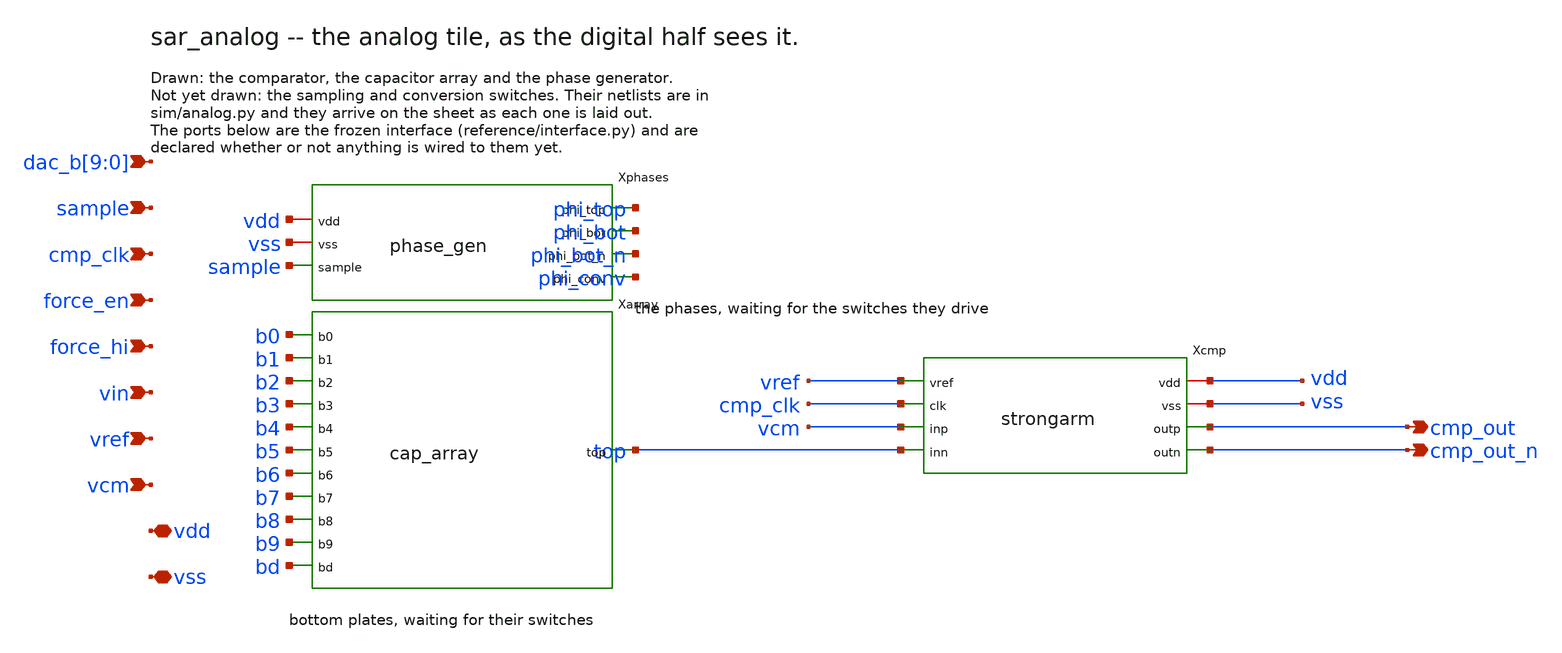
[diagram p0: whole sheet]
** sch_path: xschem/sar_analog.sch
**.subckt sar_analog
*+ dac_b[9],dac_b[8],dac_b[7],dac_b[6],dac_b[5],dac_b[4],dac_b[3],dac_b[2],dac_b[1],dac_b[0] sample cmp_clk force_en force_hi vin vref vcm vdd vss cmp_out cmp_out_n
*.ipin dac_b[9],dac_b[8],dac_b[7],dac_b[6],dac_b[5],dac_b[4],dac_b[3],dac_b[2],dac_b[1],dac_b[0]
*.ipin sample
*.ipin cmp_clk
*.ipin force_en
*.ipin force_hi
*.ipin vin
*.ipin vref
*.ipin vcm
*.iopin vdd
*.iopin vss
*.opin cmp_out
*.opin cmp_out_n
Xcmp vdd vss vref cmp_clk vcm top cmp_out cmp_out_n strongarm
Xphases vdd vss sample phi_top phi_bot phi_bot_n phi_conv phase_gen
Xarray top b0 b1 b2 b3 b4 b5 b6 b7 b8 b9 bd cap_array
**.ends

* expanding   symbol:  strongarm.sym # of pins=8
** sym_path: xschem/strongarm.sym
** sch_path: xschem/strongarm.sch
.subckt strongarm vdd vss vref clk inp inn outp outn
*.iopin vdd
*.iopin vss
*.ipin vref
*.ipin clk
*.ipin inp
*.ipin inn
*.opin outp
*.opin outn
Xinvp clk_i clk vdd vdd sky130_fd_pr__pfet_01v8 L=0.15 W=2 nf=1 ad='int((nf+1)/2) * W/nf * 0.29' as='int((nf+2)/2) * W/nf * 0.29'
+ pd='2*int((nf+1)/2) * (W/nf + 0.29)' ps='2*int((nf+2)/2) * (W/nf + 0.29)' nrd='0.29 / W' nrs='0.29 / W'
+ sa=0 sb=0 sd=0 mult=1 m=1
Xinvn clk_i clk vss vss sky130_fd_pr__nfet_01v8 L=0.15 W=2 nf=1 ad='int((1 + 1)/2) * 2 / 1 * 0.29' as='int((1 + 2)/2) * 2 / 1 * 0.29'
+ pd='2*int((1 + 1)/2) * (2 / 1 + 0.29)' ps='2*int((1 + 2)/2) * (2 / 1 + 0.29)' nrd='0.29 / 2 ' nrs='0.29 / 2 '
+ sa=0 sb=0 sd=0 mult=1 m=1
Xbref bias vref vss vss sky130_fd_pr__nfet_01v8 L=2 W=1 nf=1 ad='int((1 + 1)/2) * 1 / 1 * 0.29' as='int((1 + 2)/2) * 1 / 1 * 0.29'
+ pd='2*int((1 + 1)/2) * (1 / 1 + 0.29)' ps='2*int((1 + 2)/2) * (1 / 1 + 0.29)' nrd='0.29 / 1 ' nrs='0.29 / 1 '
+ sa=0 sb=0 sd=0 mult=1 m=1
Xbdio bias bias vdd vdd sky130_fd_pr__pfet_01v8 L=0.5 W=1 nf=1 ad='int((nf+1)/2) * W/nf * 0.29' as='int((nf+2)/2) * W/nf * 0.29'
+ pd='2*int((nf+1)/2) * (W/nf + 0.29)' ps='2*int((nf+2)/2) * (W/nf + 0.29)' nrd='0.29 / W' nrs='0.29 / W'
+ sa=0 sb=0 sd=0 mult=1 m=1
Xbgoff tgate clk vdd vdd sky130_fd_pr__pfet_01v8 L=0.15 W=1 nf=1 ad='int((nf+1)/2) * W/nf * 0.29' as='int((nf+2)/2) * W/nf * 0.29'
+ pd='2*int((nf+1)/2) * (W/nf + 0.29)' ps='2*int((nf+2)/2) * (W/nf + 0.29)' nrd='0.29 / W' nrs='0.29 / W'
+ sa=0 sb=0 sd=0 mult=1 m=1
Xbgon bias clk tgate vss sky130_fd_pr__nfet_01v8 L=0.15 W=1 nf=1 ad='int((1 + 1)/2) * 1 / 1 * 0.29' as='int((1 + 2)/2) * 1 / 1 * 0.29'
+ pd='2*int((1 + 1)/2) * (1 / 1 + 0.29)' ps='2*int((1 + 2)/2) * (1 / 1 + 0.29)' nrd='0.29 / 1 ' nrs='0.29 / 1 '
+ sa=0 sb=0 sd=0 mult=1 m=1
Cbias bias vss 1e-13 m=1
Xtail tail tgate vdd vdd sky130_fd_pr__pfet_01v8 L=0.5 W=2 nf=1 ad='int((nf+1)/2) * W/nf * 0.29' as='int((nf+2)/2) * W/nf * 0.29'
+ pd='2*int((nf+1)/2) * (W/nf + 0.29)' ps='2*int((nf+2)/2) * (W/nf + 0.29)' nrd='0.29 / W' nrs='0.29 / W'
+ sa=0 sb=0 sd=0 mult=1 m=1
Xinp xn inp tail vdd sky130_fd_pr__pfet_01v8 L=0.5 W=4 nf=1 ad='int((nf+1)/2) * W/nf * 0.29' as='int((nf+2)/2) * W/nf * 0.29'
+ pd='2*int((nf+1)/2) * (W/nf + 0.29)' ps='2*int((nf+2)/2) * (W/nf + 0.29)' nrd='0.29 / W' nrs='0.29 / W'
+ sa=0 sb=0 sd=0 mult=1 m=1
Xinn xp inn tail vdd sky130_fd_pr__pfet_01v8 L=0.5 W=4 nf=1 ad='int((nf+1)/2) * W/nf * 0.29' as='int((nf+2)/2) * W/nf * 0.29'
+ pd='2*int((nf+1)/2) * (W/nf + 0.29)' ps='2*int((nf+2)/2) * (W/nf + 0.29)' nrd='0.29 / W' nrs='0.29 / W'
+ sa=0 sb=0 sd=0 mult=1 m=1
Xlchp outp outn xp vdd sky130_fd_pr__pfet_01v8 L=0.15 W=1 nf=1 ad='int((nf+1)/2) * W/nf * 0.29' as='int((nf+2)/2) * W/nf * 0.29'
+ pd='2*int((nf+1)/2) * (W/nf + 0.29)' ps='2*int((nf+2)/2) * (W/nf + 0.29)' nrd='0.29 / W' nrs='0.29 / W'
+ sa=0 sb=0 sd=0 mult=1 m=1
Xlchn outn outp xn vdd sky130_fd_pr__pfet_01v8 L=0.15 W=1 nf=1 ad='int((nf+1)/2) * W/nf * 0.29' as='int((nf+2)/2) * W/nf * 0.29'
+ pd='2*int((nf+1)/2) * (W/nf + 0.29)' ps='2*int((nf+2)/2) * (W/nf + 0.29)' nrd='0.29 / W' nrs='0.29 / W'
+ sa=0 sb=0 sd=0 mult=1 m=1
Xldp outp outn vss vss sky130_fd_pr__nfet_01v8 L=0.15 W=2 nf=1 ad='int((1 + 1)/2) * 2 / 1 * 0.29' as='int((1 + 2)/2) * 2 / 1 * 0.29'
+ pd='2*int((1 + 1)/2) * (2 / 1 + 0.29)' ps='2*int((1 + 2)/2) * (2 / 1 + 0.29)' nrd='0.29 / 2 ' nrs='0.29 / 2 '
+ sa=0 sb=0 sd=0 mult=1 m=1
Xldn outn outp vss vss sky130_fd_pr__nfet_01v8 L=0.15 W=2 nf=1 ad='int((1 + 1)/2) * 2 / 1 * 0.29' as='int((1 + 2)/2) * 2 / 1 * 0.29'
+ pd='2*int((1 + 1)/2) * (2 / 1 + 0.29)' ps='2*int((1 + 2)/2) * (2 / 1 + 0.29)' nrd='0.29 / 2 ' nrs='0.29 / 2 '
+ sa=0 sb=0 sd=0 mult=1 m=1
Xprep outp clk_i vss vss sky130_fd_pr__nfet_01v8 L=0.15 W=2 nf=1 ad='int((1 + 1)/2) * 2 / 1 * 0.29' as='int((1 + 2)/2) * 2 / 1 * 0.29'
+ pd='2*int((1 + 1)/2) * (2 / 1 + 0.29)' ps='2*int((1 + 2)/2) * (2 / 1 + 0.29)' nrd='0.29 / 2 ' nrs='0.29 / 2 '
+ sa=0 sb=0 sd=0 mult=1 m=1
Xpren outn clk_i vss vss sky130_fd_pr__nfet_01v8 L=0.15 W=2 nf=1 ad='int((1 + 1)/2) * 2 / 1 * 0.29' as='int((1 + 2)/2) * 2 / 1 * 0.29'
+ pd='2*int((1 + 1)/2) * (2 / 1 + 0.29)' ps='2*int((1 + 2)/2) * (2 / 1 + 0.29)' nrd='0.29 / 2 ' nrs='0.29 / 2 '
+ sa=0 sb=0 sd=0 mult=1 m=1
Xprxp xp clk_i vss vss sky130_fd_pr__nfet_01v8 L=0.15 W=2 nf=1 ad='int((1 + 1)/2) * 2 / 1 * 0.29' as='int((1 + 2)/2) * 2 / 1 * 0.29'
+ pd='2*int((1 + 1)/2) * (2 / 1 + 0.29)' ps='2*int((1 + 2)/2) * (2 / 1 + 0.29)' nrd='0.29 / 2 ' nrs='0.29 / 2 '
+ sa=0 sb=0 sd=0 mult=1 m=1
Xprxn xn clk_i vss vss sky130_fd_pr__nfet_01v8 L=0.15 W=2 nf=1 ad='int((1 + 1)/2) * 2 / 1 * 0.29' as='int((1 + 2)/2) * 2 / 1 * 0.29'
+ pd='2*int((1 + 1)/2) * (2 / 1 + 0.29)' ps='2*int((1 + 2)/2) * (2 / 1 + 0.29)' nrd='0.29 / 2 ' nrs='0.29 / 2 '
+ sa=0 sb=0 sd=0 mult=1 m=1
Cxp xp vss 2e-13 m=1
Cxn xn vss 2e-13 m=1
Coutp outp vss 1e-14 m=1
Coutn outn vss 1e-14 m=1
.ends


* expanding   symbol:  phase_gen.sym # of pins=7
** sym_path: xschem/phase_gen.sym
** sch_path: xschem/phase_gen.sch
.subckt phase_gen vdd vss sample phi_top phi_bot phi_bot_n phi_conv
*.iopin vdd
*.iopin vss
*.ipin sample
*.opin phi_top
*.opin phi_bot
*.opin phi_bot_n
*.opin phi_conv
Xbtop0p btop_s0 sample vdd vdd sky130_fd_pr__pfet_01v8 L=0.15 W=1 nf=1 ad='int((nf+1)/2) * W/nf * 0.29'
+ as='int((nf+2)/2) * W/nf * 0.29' pd='2*int((nf+1)/2) * (W/nf + 0.29)' ps='2*int((nf+2)/2) * (W/nf + 0.29)'
+ nrd='0.29 / W' nrs='0.29 / W' sa=0 sb=0 sd=0 mult=1 m=1
Xbtop0n btop_s0 sample vss vss sky130_fd_pr__nfet_01v8 L=0.15 W=0.5 nf=1 ad='int((1 + 1)/2) * 0.5 / 1 * 0.29'
+ as='int((1 + 2)/2) * 0.5 / 1 * 0.29' pd='2*int((1 + 1)/2) * (0.5 / 1 + 0.29)' ps='2*int((1 + 2)/2) * (0.5 / 1 + 0.29)'
+ nrd='0.29 / 0.5 ' nrs='0.29 / 0.5 ' sa=0 sb=0 sd=0 mult=1 m=1
Xbtop1p phi_top btop_s0 vdd vdd sky130_fd_pr__pfet_01v8 L=0.15 W=4 nf=1 ad='int((nf+1)/2) * W/nf * 0.29'
+ as='int((nf+2)/2) * W/nf * 0.29' pd='2*int((nf+1)/2) * (W/nf + 0.29)' ps='2*int((nf+2)/2) * (W/nf + 0.29)'
+ nrd='0.29 / W' nrs='0.29 / W' sa=0 sb=0 sd=0 mult=1 m=1
Xbtop1n phi_top btop_s0 vss vss sky130_fd_pr__nfet_01v8 L=0.15 W=2 nf=1 ad='int((1 + 1)/2) * 2 / 1 * 0.29'
+ as='int((1 + 2)/2) * 2 / 1 * 0.29' pd='2*int((1 + 1)/2) * (2 / 1 + 0.29)' ps='2*int((1 + 2)/2) * (2 / 1 + 0.29)'
+ nrd='0.29 / 2 ' nrs='0.29 / 2 ' sa=0 sb=0 sd=0 mult=1 m=1
Xstopsp stop_lo phi_top vdd vdd sky130_fd_pr__pfet_01v8 L=1 W=0.42 nf=1 ad='int((nf+1)/2) * W/nf * 0.29'
+ as='int((nf+2)/2) * W/nf * 0.29' pd='2*int((nf+1)/2) * (W/nf + 0.29)' ps='2*int((nf+2)/2) * (W/nf + 0.29)'
+ nrd='0.29 / W' nrs='0.29 / W' sa=0 sb=0 sd=0 mult=1 m=1
Xstopsn stop_lo phi_top vss vss sky130_fd_pr__nfet_01v8 L=0.15 W=2 nf=1 ad='int((1 + 1)/2) * 2 / 1 * 0.29'
+ as='int((1 + 2)/2) * 2 / 1 * 0.29' pd='2*int((1 + 1)/2) * (2 / 1 + 0.29)' ps='2*int((1 + 2)/2) * (2 / 1 + 0.29)'
+ nrd='0.29 / 2 ' nrs='0.29 / 2 ' sa=0 sb=0 sd=0 mult=1 m=1
Xstoprp top_on stop_lo vdd vdd sky130_fd_pr__pfet_01v8 L=0.15 W=1 nf=1 ad='int((nf+1)/2) * W/nf * 0.29'
+ as='int((nf+2)/2) * W/nf * 0.29' pd='2*int((nf+1)/2) * (W/nf + 0.29)' ps='2*int((nf+2)/2) * (W/nf + 0.29)'
+ nrd='0.29 / W' nrs='0.29 / W' sa=0 sb=0 sd=0 mult=1 m=1
Xstoprn top_on stop_lo vss vss sky130_fd_pr__nfet_01v8 L=0.15 W=0.5 nf=1 ad='int((1 + 1)/2) * 0.5 / 1 * 0.29'
+ as='int((1 + 2)/2) * 0.5 / 1 * 0.29' pd='2*int((1 + 1)/2) * (0.5 / 1 + 0.29)' ps='2*int((1 + 2)/2) * (0.5 / 1 + 0.29)'
+ nrd='0.29 / 0.5 ' nrs='0.29 / 0.5 ' sa=0 sb=0 sd=0 mult=1 m=1
Xnor_heldp0 nor_held_m0 sample vdd vdd sky130_fd_pr__pfet_01v8 L=0.15 W=2 nf=1 ad='int((nf+1)/2) * W/nf * 0.29'
+ as='int((nf+2)/2) * W/nf * 0.29' pd='2*int((nf+1)/2) * (W/nf + 0.29)' ps='2*int((nf+2)/2) * (W/nf + 0.29)'
+ nrd='0.29 / W' nrs='0.29 / W' sa=0 sb=0 sd=0 mult=1 m=1
Xnor_heldp1 held_n top_on nor_held_m0 vdd sky130_fd_pr__pfet_01v8 L=0.15 W=2 nf=1 ad='int((nf+1)/2) * W/nf * 0.29'
+ as='int((nf+2)/2) * W/nf * 0.29' pd='2*int((nf+1)/2) * (W/nf + 0.29)' ps='2*int((nf+2)/2) * (W/nf + 0.29)'
+ nrd='0.29 / W' nrs='0.29 / W' sa=0 sb=0 sd=0 mult=1 m=1
Xnor_heldn0 held_n sample vss vss sky130_fd_pr__nfet_01v8 L=0.15 W=0.5 nf=1 ad='int((1 + 1)/2) * 0.5 / 1 * 0.29'
+ as='int((1 + 2)/2) * 0.5 / 1 * 0.29' pd='2*int((1 + 1)/2) * (0.5 / 1 + 0.29)' ps='2*int((1 + 2)/2) * (0.5 / 1 + 0.29)'
+ nrd='0.29 / 0.5 ' nrs='0.29 / 0.5 ' sa=0 sb=0 sd=0 mult=1 m=1
Xnor_heldn1 held_n top_on vss vss sky130_fd_pr__nfet_01v8 L=0.15 W=0.5 nf=1 ad='int((1 + 1)/2) * 0.5 / 1 * 0.29'
+ as='int((1 + 2)/2) * 0.5 / 1 * 0.29' pd='2*int((1 + 1)/2) * (0.5 / 1 + 0.29)' ps='2*int((1 + 2)/2) * (0.5 / 1 + 0.29)'
+ nrd='0.29 / 0.5 ' nrs='0.29 / 0.5 ' sa=0 sb=0 sd=0 mult=1 m=1
Xnor_botp0 nor_bot_m0 held_n vdd vdd sky130_fd_pr__pfet_01v8 L=0.15 W=2 nf=1 ad='int((nf+1)/2) * W/nf * 0.29'
+ as='int((nf+2)/2) * W/nf * 0.29' pd='2*int((nf+1)/2) * (W/nf + 0.29)' ps='2*int((nf+2)/2) * (W/nf + 0.29)'
+ nrd='0.29 / W' nrs='0.29 / W' sa=0 sb=0 sd=0 mult=1 m=1
Xnor_botp1 bot_pre cnv_on nor_bot_m0 vdd sky130_fd_pr__pfet_01v8 L=0.15 W=2 nf=1 ad='int((nf+1)/2) * W/nf * 0.29'
+ as='int((nf+2)/2) * W/nf * 0.29' pd='2*int((nf+1)/2) * (W/nf + 0.29)' ps='2*int((nf+2)/2) * (W/nf + 0.29)'
+ nrd='0.29 / W' nrs='0.29 / W' sa=0 sb=0 sd=0 mult=1 m=1
Xnor_botn0 bot_pre held_n vss vss sky130_fd_pr__nfet_01v8 L=0.15 W=0.5 nf=1 ad='int((1 + 1)/2) * 0.5 / 1 * 0.29'
+ as='int((1 + 2)/2) * 0.5 / 1 * 0.29' pd='2*int((1 + 1)/2) * (0.5 / 1 + 0.29)' ps='2*int((1 + 2)/2) * (0.5 / 1 + 0.29)'
+ nrd='0.29 / 0.5 ' nrs='0.29 / 0.5 ' sa=0 sb=0 sd=0 mult=1 m=1
Xnor_botn1 bot_pre cnv_on vss vss sky130_fd_pr__nfet_01v8 L=0.15 W=0.5 nf=1 ad='int((1 + 1)/2) * 0.5 / 1 * 0.29'
+ as='int((1 + 2)/2) * 0.5 / 1 * 0.29' pd='2*int((1 + 1)/2) * (0.5 / 1 + 0.29)' ps='2*int((1 + 2)/2) * (0.5 / 1 + 0.29)'
+ nrd='0.29 / 0.5 ' nrs='0.29 / 0.5 ' sa=0 sb=0 sd=0 mult=1 m=1
Xbbot0p bbot_s0 bot_pre vdd vdd sky130_fd_pr__pfet_01v8 L=0.15 W=1 nf=1 ad='int((nf+1)/2) * W/nf * 0.29'
+ as='int((nf+2)/2) * W/nf * 0.29' pd='2*int((nf+1)/2) * (W/nf + 0.29)' ps='2*int((nf+2)/2) * (W/nf + 0.29)'
+ nrd='0.29 / W' nrs='0.29 / W' sa=0 sb=0 sd=0 mult=1 m=1
Xbbot0n bbot_s0 bot_pre vss vss sky130_fd_pr__nfet_01v8 L=0.15 W=0.5 nf=1 ad='int((1 + 1)/2) * 0.5 / 1 * 0.29'
+ as='int((1 + 2)/2) * 0.5 / 1 * 0.29' pd='2*int((1 + 1)/2) * (0.5 / 1 + 0.29)' ps='2*int((1 + 2)/2) * (0.5 / 1 + 0.29)'
+ nrd='0.29 / 0.5 ' nrs='0.29 / 0.5 ' sa=0 sb=0 sd=0 mult=1 m=1
Xbbot1p bbot_s1 bbot_s0 vdd vdd sky130_fd_pr__pfet_01v8 L=0.15 W=4 nf=1 ad='int((nf+1)/2) * W/nf * 0.29'
+ as='int((nf+2)/2) * W/nf * 0.29' pd='2*int((nf+1)/2) * (W/nf + 0.29)' ps='2*int((nf+2)/2) * (W/nf + 0.29)'
+ nrd='0.29 / W' nrs='0.29 / W' sa=0 sb=0 sd=0 mult=1 m=1
Xbbot1n bbot_s1 bbot_s0 vss vss sky130_fd_pr__nfet_01v8 L=0.15 W=2 nf=1 ad='int((1 + 1)/2) * 2 / 1 * 0.29'
+ as='int((1 + 2)/2) * 2 / 1 * 0.29' pd='2*int((1 + 1)/2) * (2 / 1 + 0.29)' ps='2*int((1 + 2)/2) * (2 / 1 + 0.29)'
+ nrd='0.29 / 2 ' nrs='0.29 / 2 ' sa=0 sb=0 sd=0 mult=1 m=1
Xbbot2p bbot_s2 bbot_s1 vdd vdd sky130_fd_pr__pfet_01v8 L=0.15 W=4 nf=1 ad='int((nf+1)/2) * W/nf * 0.29'
+ as='int((nf+2)/2) * W/nf * 0.29' pd='2*int((nf+1)/2) * (W/nf + 0.29)' ps='2*int((nf+2)/2) * (W/nf + 0.29)'
+ nrd='0.29 / W' nrs='0.29 / W' sa=0 sb=0 sd=0 mult=4 m=4
Xbbot2n bbot_s2 bbot_s1 vss vss sky130_fd_pr__nfet_01v8 L=0.15 W=4 nf=1 ad='int((1 + 1)/2) * 4 / 1 * 0.29'
+ as='int((1 + 2)/2) * 4 / 1 * 0.29' pd='2*int((1 + 1)/2) * (4 / 1 + 0.29)' ps='2*int((1 + 2)/2) * (4 / 1 + 0.29)'
+ nrd='0.29 / 4 ' nrs='0.29 / 4 ' sa=0 sb=0 sd=0 mult=2 m=2
Xbbot3p phi_bot bbot_s2 vdd vdd sky130_fd_pr__pfet_01v8 L=0.15 W=4.92308 nf=1 ad='int((nf+1)/2) * W/nf * 0.29'
+ as='int((nf+2)/2) * W/nf * 0.29' pd='2*int((nf+1)/2) * (W/nf + 0.29)' ps='2*int((nf+2)/2) * (W/nf + 0.29)'
+ nrd='0.29 / W' nrs='0.29 / W' sa=0 sb=0 sd=0 mult=13 m=13
Xbbot3n phi_bot bbot_s2 vss vss sky130_fd_pr__nfet_01v8 L=0.15 W=4.57143 nf=1 ad='int((1 + 1)/2) * 4.57143 / 1 * 0.29'
+ as='int((1 + 2)/2) * 4.57143 / 1 * 0.29' pd='2*int((1 + 1)/2) * (4.57143 / 1 + 0.29)' ps='2*int((1 + 2)/2) * (4.57143 / 1 + 0.29)'
+ nrd='0.29 / 4.57143 ' nrs='0.29 / 4.57143 ' sa=0 sb=0 sd=0 mult=7 m=7
Xsbotsp sbot_lo phi_bot vdd vdd sky130_fd_pr__pfet_01v8 L=1 W=0.42 nf=1 ad='int((nf+1)/2) * W/nf * 0.29'
+ as='int((nf+2)/2) * W/nf * 0.29' pd='2*int((nf+1)/2) * (W/nf + 0.29)' ps='2*int((nf+2)/2) * (W/nf + 0.29)'
+ nrd='0.29 / W' nrs='0.29 / W' sa=0 sb=0 sd=0 mult=1 m=1
Xsbotsn sbot_lo phi_bot vss vss sky130_fd_pr__nfet_01v8 L=0.15 W=2 nf=1 ad='int((1 + 1)/2) * 2 / 1 * 0.29'
+ as='int((1 + 2)/2) * 2 / 1 * 0.29' pd='2*int((1 + 1)/2) * (2 / 1 + 0.29)' ps='2*int((1 + 2)/2) * (2 / 1 + 0.29)'
+ nrd='0.29 / 2 ' nrs='0.29 / 2 ' sa=0 sb=0 sd=0 mult=1 m=1
Xsbotrp bot_on sbot_lo vdd vdd sky130_fd_pr__pfet_01v8 L=0.15 W=1 nf=1 ad='int((nf+1)/2) * W/nf * 0.29'
+ as='int((nf+2)/2) * W/nf * 0.29' pd='2*int((nf+1)/2) * (W/nf + 0.29)' ps='2*int((nf+2)/2) * (W/nf + 0.29)'
+ nrd='0.29 / W' nrs='0.29 / W' sa=0 sb=0 sd=0 mult=1 m=1
Xsbotrn bot_on sbot_lo vss vss sky130_fd_pr__nfet_01v8 L=0.15 W=0.5 nf=1 ad='int((1 + 1)/2) * 0.5 / 1 * 0.29'
+ as='int((1 + 2)/2) * 0.5 / 1 * 0.29' pd='2*int((1 + 1)/2) * (0.5 / 1 + 0.29)' ps='2*int((1 + 2)/2) * (0.5 / 1 + 0.29)'
+ nrd='0.29 / 0.5 ' nrs='0.29 / 0.5 ' sa=0 sb=0 sd=0 mult=1 m=1
Xbbotn0p bbotn_s0 bot_pre vdd vdd sky130_fd_pr__pfet_01v8 L=0.15 W=4 nf=1 ad='int((nf+1)/2) * W/nf * 0.29'
+ as='int((nf+2)/2) * W/nf * 0.29' pd='2*int((nf+1)/2) * (W/nf + 0.29)' ps='2*int((nf+2)/2) * (W/nf + 0.29)'
+ nrd='0.29 / W' nrs='0.29 / W' sa=0 sb=0 sd=0 mult=1 m=1
Xbbotn0n bbotn_s0 bot_pre vss vss sky130_fd_pr__nfet_01v8 L=0.15 W=2 nf=1 ad='int((1 + 1)/2) * 2 / 1 * 0.29'
+ as='int((1 + 2)/2) * 2 / 1 * 0.29' pd='2*int((1 + 1)/2) * (2 / 1 + 0.29)' ps='2*int((1 + 2)/2) * (2 / 1 + 0.29)'
+ nrd='0.29 / 2 ' nrs='0.29 / 2 ' sa=0 sb=0 sd=0 mult=1 m=1
Xbbotn1p bbotn_s1 bbotn_s0 vdd vdd sky130_fd_pr__pfet_01v8 L=0.15 W=4 nf=1 ad='int((nf+1)/2) * W/nf * 0.29'
+ as='int((nf+2)/2) * W/nf * 0.29' pd='2*int((nf+1)/2) * (W/nf + 0.29)' ps='2*int((nf+2)/2) * (W/nf + 0.29)'
+ nrd='0.29 / W' nrs='0.29 / W' sa=0 sb=0 sd=0 mult=4 m=4
Xbbotn1n bbotn_s1 bbotn_s0 vss vss sky130_fd_pr__nfet_01v8 L=0.15 W=4 nf=1 ad='int((1 + 1)/2) * 4 / 1 * 0.29'
+ as='int((1 + 2)/2) * 4 / 1 * 0.29' pd='2*int((1 + 1)/2) * (4 / 1 + 0.29)' ps='2*int((1 + 2)/2) * (4 / 1 + 0.29)'
+ nrd='0.29 / 4 ' nrs='0.29 / 4 ' sa=0 sb=0 sd=0 mult=2 m=2
Xbbotn2p phi_bot_n bbotn_s1 vdd vdd sky130_fd_pr__pfet_01v8 L=0.15 W=4.92308 nf=1 ad='int((nf+1)/2) * W/nf * 0.29'
+ as='int((nf+2)/2) * W/nf * 0.29' pd='2*int((nf+1)/2) * (W/nf + 0.29)' ps='2*int((nf+2)/2) * (W/nf + 0.29)'
+ nrd='0.29 / W' nrs='0.29 / W' sa=0 sb=0 sd=0 mult=13 m=13
Xbbotn2n phi_bot_n bbotn_s1 vss vss sky130_fd_pr__nfet_01v8 L=0.15 W=4.57143 nf=1 ad='int((1 + 1)/2) * 4.57143 / 1 * 0.29'
+ as='int((1 + 2)/2) * 4.57143 / 1 * 0.29' pd='2*int((1 + 1)/2) * (4.57143 / 1 + 0.29)' ps='2*int((1 + 2)/2) * (4.57143 / 1 + 0.29)'
+ nrd='0.29 / 4.57143 ' nrs='0.29 / 4.57143 ' sa=0 sb=0 sd=0 mult=7 m=7
Xsbotnsp sbotn_hi phi_bot_n vdd vdd sky130_fd_pr__pfet_01v8 L=0.15 W=4 nf=1 ad='int((nf+1)/2) * W/nf * 0.29'
+ as='int((nf+2)/2) * W/nf * 0.29' pd='2*int((nf+1)/2) * (W/nf + 0.29)' ps='2*int((nf+2)/2) * (W/nf + 0.29)'
+ nrd='0.29 / W' nrs='0.29 / W' sa=0 sb=0 sd=0 mult=1 m=1
Xsbotnsn sbotn_hi phi_bot_n vss vss sky130_fd_pr__nfet_01v8 L=1 W=0.42 nf=1 ad='int((1 + 1)/2) * 0.42 / 1 * 0.29'
+ as='int((1 + 2)/2) * 0.42 / 1 * 0.29' pd='2*int((1 + 1)/2) * (0.42 / 1 + 0.29)' ps='2*int((1 + 2)/2) * (0.42 / 1 + 0.29)'
+ nrd='0.29 / 0.42 ' nrs='0.29 / 0.42 ' sa=0 sb=0 sd=0 mult=1 m=1
Xsbotnr0p sbotnr_s0 sbotn_hi vdd vdd sky130_fd_pr__pfet_01v8 L=0.15 W=1 nf=1 ad='int((nf+1)/2) * W/nf * 0.29'
+ as='int((nf+2)/2) * W/nf * 0.29' pd='2*int((nf+1)/2) * (W/nf + 0.29)' ps='2*int((nf+2)/2) * (W/nf + 0.29)'
+ nrd='0.29 / W' nrs='0.29 / W' sa=0 sb=0 sd=0 mult=1 m=1
Xsbotnr0n sbotnr_s0 sbotn_hi vss vss sky130_fd_pr__nfet_01v8 L=0.15 W=0.5 nf=1 ad='int((1 + 1)/2) * 0.5 / 1 * 0.29'
+ as='int((1 + 2)/2) * 0.5 / 1 * 0.29' pd='2*int((1 + 1)/2) * (0.5 / 1 + 0.29)' ps='2*int((1 + 2)/2) * (0.5 / 1 + 0.29)'
+ nrd='0.29 / 0.5 ' nrs='0.29 / 0.5 ' sa=0 sb=0 sd=0 mult=1 m=1
Xsbotnr1p botn_on sbotnr_s0 vdd vdd sky130_fd_pr__pfet_01v8 L=0.15 W=4 nf=1 ad='int((nf+1)/2) * W/nf * 0.29'
+ as='int((nf+2)/2) * W/nf * 0.29' pd='2*int((nf+1)/2) * (W/nf + 0.29)' ps='2*int((nf+2)/2) * (W/nf + 0.29)'
+ nrd='0.29 / W' nrs='0.29 / W' sa=0 sb=0 sd=0 mult=1 m=1
Xsbotnr1n botn_on sbotnr_s0 vss vss sky130_fd_pr__nfet_01v8 L=0.15 W=2 nf=1 ad='int((1 + 1)/2) * 2 / 1 * 0.29'
+ as='int((1 + 2)/2) * 2 / 1 * 0.29' pd='2*int((1 + 1)/2) * (2 / 1 + 0.29)' ps='2*int((1 + 2)/2) * (2 / 1 + 0.29)'
+ nrd='0.29 / 2 ' nrs='0.29 / 2 ' sa=0 sb=0 sd=0 mult=1 m=1
Xnor_cnvp0 nor_cnv_m0 sample vdd vdd sky130_fd_pr__pfet_01v8 L=0.15 W=3 nf=1 ad='int((nf+1)/2) * W/nf * 0.29'
+ as='int((nf+2)/2) * W/nf * 0.29' pd='2*int((nf+1)/2) * (W/nf + 0.29)' ps='2*int((nf+2)/2) * (W/nf + 0.29)'
+ nrd='0.29 / W' nrs='0.29 / W' sa=0 sb=0 sd=0 mult=1 m=1
Xnor_cnvp1 nor_cnv_m1 bot_on nor_cnv_m0 vdd sky130_fd_pr__pfet_01v8 L=0.15 W=3 nf=1 ad='int((nf+1)/2) * W/nf * 0.29'
+ as='int((nf+2)/2) * W/nf * 0.29' pd='2*int((nf+1)/2) * (W/nf + 0.29)' ps='2*int((nf+2)/2) * (W/nf + 0.29)'
+ nrd='0.29 / W' nrs='0.29 / W' sa=0 sb=0 sd=0 mult=1 m=1
Xnor_cnvp2 cnv_pre botn_on nor_cnv_m1 vdd sky130_fd_pr__pfet_01v8 L=0.15 W=3 nf=1 ad='int((nf+1)/2) * W/nf * 0.29'
+ as='int((nf+2)/2) * W/nf * 0.29' pd='2*int((nf+1)/2) * (W/nf + 0.29)' ps='2*int((nf+2)/2) * (W/nf + 0.29)'
+ nrd='0.29 / W' nrs='0.29 / W' sa=0 sb=0 sd=0 mult=1 m=1
Xnor_cnvn0 cnv_pre sample vss vss sky130_fd_pr__nfet_01v8 L=0.15 W=0.5 nf=1 ad='int((1 + 1)/2) * 0.5 / 1 * 0.29'
+ as='int((1 + 2)/2) * 0.5 / 1 * 0.29' pd='2*int((1 + 1)/2) * (0.5 / 1 + 0.29)' ps='2*int((1 + 2)/2) * (0.5 / 1 + 0.29)'
+ nrd='0.29 / 0.5 ' nrs='0.29 / 0.5 ' sa=0 sb=0 sd=0 mult=1 m=1
Xnor_cnvn1 cnv_pre bot_on vss vss sky130_fd_pr__nfet_01v8 L=0.15 W=0.5 nf=1 ad='int((1 + 1)/2) * 0.5 / 1 * 0.29'
+ as='int((1 + 2)/2) * 0.5 / 1 * 0.29' pd='2*int((1 + 1)/2) * (0.5 / 1 + 0.29)' ps='2*int((1 + 2)/2) * (0.5 / 1 + 0.29)'
+ nrd='0.29 / 0.5 ' nrs='0.29 / 0.5 ' sa=0 sb=0 sd=0 mult=1 m=1
Xnor_cnvn2 cnv_pre botn_on vss vss sky130_fd_pr__nfet_01v8 L=0.15 W=0.5 nf=1 ad='int((1 + 1)/2) * 0.5 / 1 * 0.29'
+ as='int((1 + 2)/2) * 0.5 / 1 * 0.29' pd='2*int((1 + 1)/2) * (0.5 / 1 + 0.29)' ps='2*int((1 + 2)/2) * (0.5 / 1 + 0.29)'
+ nrd='0.29 / 0.5 ' nrs='0.29 / 0.5 ' sa=0 sb=0 sd=0 mult=1 m=1
Xbcnv0p bcnv_s0 cnv_pre vdd vdd sky130_fd_pr__pfet_01v8 L=0.15 W=1 nf=1 ad='int((nf+1)/2) * W/nf * 0.29'
+ as='int((nf+2)/2) * W/nf * 0.29' pd='2*int((nf+1)/2) * (W/nf + 0.29)' ps='2*int((nf+2)/2) * (W/nf + 0.29)'
+ nrd='0.29 / W' nrs='0.29 / W' sa=0 sb=0 sd=0 mult=1 m=1
Xbcnv0n bcnv_s0 cnv_pre vss vss sky130_fd_pr__nfet_01v8 L=0.15 W=0.5 nf=1 ad='int((1 + 1)/2) * 0.5 / 1 * 0.29'
+ as='int((1 + 2)/2) * 0.5 / 1 * 0.29' pd='2*int((1 + 1)/2) * (0.5 / 1 + 0.29)' ps='2*int((1 + 2)/2) * (0.5 / 1 + 0.29)'
+ nrd='0.29 / 0.5 ' nrs='0.29 / 0.5 ' sa=0 sb=0 sd=0 mult=1 m=1
Xbcnv1p phi_conv bcnv_s0 vdd vdd sky130_fd_pr__pfet_01v8 L=0.15 W=4 nf=1 ad='int((nf+1)/2) * W/nf * 0.29'
+ as='int((nf+2)/2) * W/nf * 0.29' pd='2*int((nf+1)/2) * (W/nf + 0.29)' ps='2*int((nf+2)/2) * (W/nf + 0.29)'
+ nrd='0.29 / W' nrs='0.29 / W' sa=0 sb=0 sd=0 mult=1 m=1
Xbcnv1n phi_conv bcnv_s0 vss vss sky130_fd_pr__nfet_01v8 L=0.15 W=2 nf=1 ad='int((1 + 1)/2) * 2 / 1 * 0.29'
+ as='int((1 + 2)/2) * 2 / 1 * 0.29' pd='2*int((1 + 1)/2) * (2 / 1 + 0.29)' ps='2*int((1 + 2)/2) * (2 / 1 + 0.29)'
+ nrd='0.29 / 2 ' nrs='0.29 / 2 ' sa=0 sb=0 sd=0 mult=1 m=1
Xscnvsp scnv_lo phi_conv vdd vdd sky130_fd_pr__pfet_01v8 L=1 W=0.42 nf=1 ad='int((nf+1)/2) * W/nf * 0.29'
+ as='int((nf+2)/2) * W/nf * 0.29' pd='2*int((nf+1)/2) * (W/nf + 0.29)' ps='2*int((nf+2)/2) * (W/nf + 0.29)'
+ nrd='0.29 / W' nrs='0.29 / W' sa=0 sb=0 sd=0 mult=1 m=1
Xscnvsn scnv_lo phi_conv vss vss sky130_fd_pr__nfet_01v8 L=0.15 W=2 nf=1 ad='int((1 + 1)/2) * 2 / 1 * 0.29'
+ as='int((1 + 2)/2) * 2 / 1 * 0.29' pd='2*int((1 + 1)/2) * (2 / 1 + 0.29)' ps='2*int((1 + 2)/2) * (2 / 1 + 0.29)'
+ nrd='0.29 / 2 ' nrs='0.29 / 2 ' sa=0 sb=0 sd=0 mult=1 m=1
Xscnvrp cnv_on scnv_lo vdd vdd sky130_fd_pr__pfet_01v8 L=0.15 W=1 nf=1 ad='int((nf+1)/2) * W/nf * 0.29'
+ as='int((nf+2)/2) * W/nf * 0.29' pd='2*int((nf+1)/2) * (W/nf + 0.29)' ps='2*int((nf+2)/2) * (W/nf + 0.29)'
+ nrd='0.29 / W' nrs='0.29 / W' sa=0 sb=0 sd=0 mult=1 m=1
Xscnvrn cnv_on scnv_lo vss vss sky130_fd_pr__nfet_01v8 L=0.15 W=0.5 nf=1 ad='int((1 + 1)/2) * 0.5 / 1 * 0.29'
+ as='int((1 + 2)/2) * 0.5 / 1 * 0.29' pd='2*int((1 + 1)/2) * (0.5 / 1 + 0.29)' ps='2*int((1 + 2)/2) * (0.5 / 1 + 0.29)'
+ nrd='0.29 / 0.5 ' nrs='0.29 / 0.5 ' sa=0 sb=0 sd=0 mult=1 m=1
.ends


* expanding   symbol:  cap_array.sym # of pins=12
** sym_path: xschem/cap_array.sym
** sch_path: xschem/cap_array.sch
.subckt cap_array top b0 b1 b2 b3 b4 b5 b6 b7 b8 b9 bd
*.iopin top
*.iopin b0
*.iopin b1
*.iopin b2
*.iopin b3
*.iopin b4
*.iopin b5
*.iopin b6
*.iopin b7
*.iopin b8
*.iopin b9
*.iopin bd
Xu0 top b0 sky130_fd_pr__cap_mim_m3_1 w=2 l=2 mult=1 m=1
Xu1 top b1 sky130_fd_pr__cap_mim_m3_1 w=2 l=2 mult=2 m=2
Xu2 top b2 sky130_fd_pr__cap_mim_m3_1 w=2 l=2 mult=4 m=4
Xu3 top b3 sky130_fd_pr__cap_mim_m3_1 w=2 l=2 mult=8 m=8
Xu4 top b4 sky130_fd_pr__cap_mim_m3_1 w=2 l=2 mult=16 m=16
Xu5 top b5 sky130_fd_pr__cap_mim_m3_1 w=2 l=2 mult=32 m=32
Xu6 top b6 sky130_fd_pr__cap_mim_m3_1 w=2 l=2 mult=64 m=64
Xu7 top b7 sky130_fd_pr__cap_mim_m3_1 w=2 l=2 mult=128 m=128
Xu8 top b8 sky130_fd_pr__cap_mim_m3_1 w=2 l=2 mult=256 m=256
Xu9 top b9 sky130_fd_pr__cap_mim_m3_1 w=2 l=2 mult=512 m=512
Xud top bd sky130_fd_pr__cap_mim_m3_1 w=2 l=2 mult=1 m=1
.ends

.end
